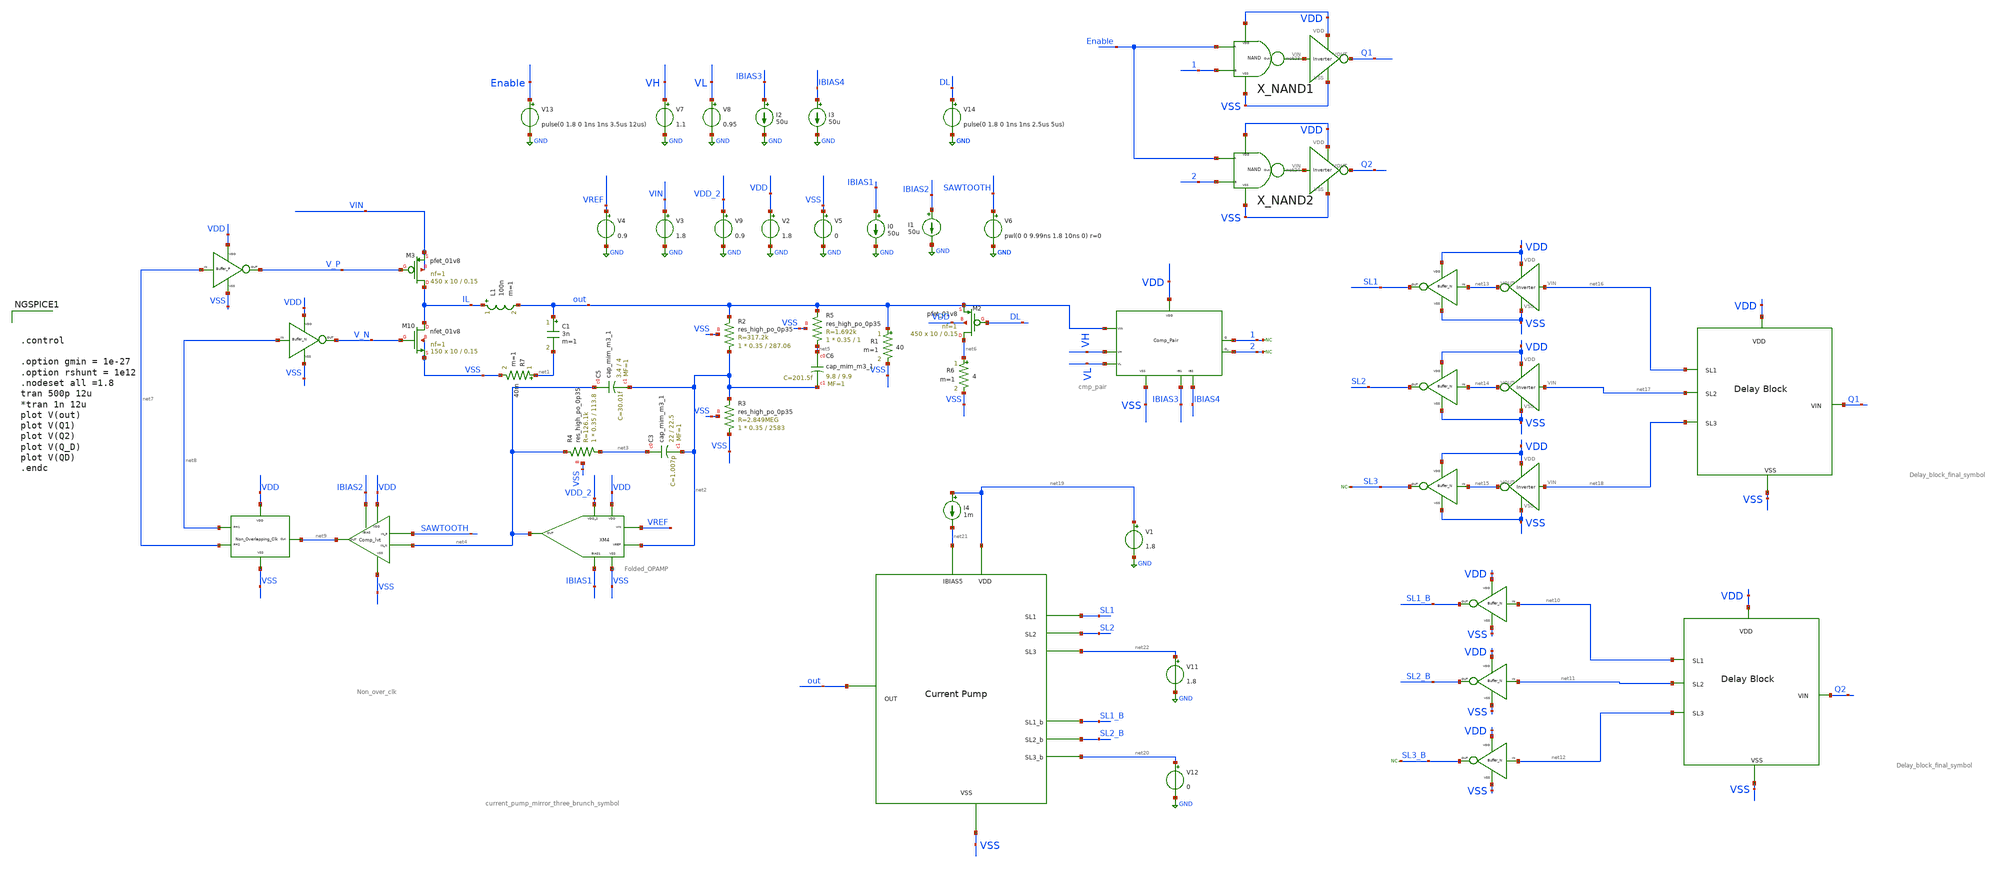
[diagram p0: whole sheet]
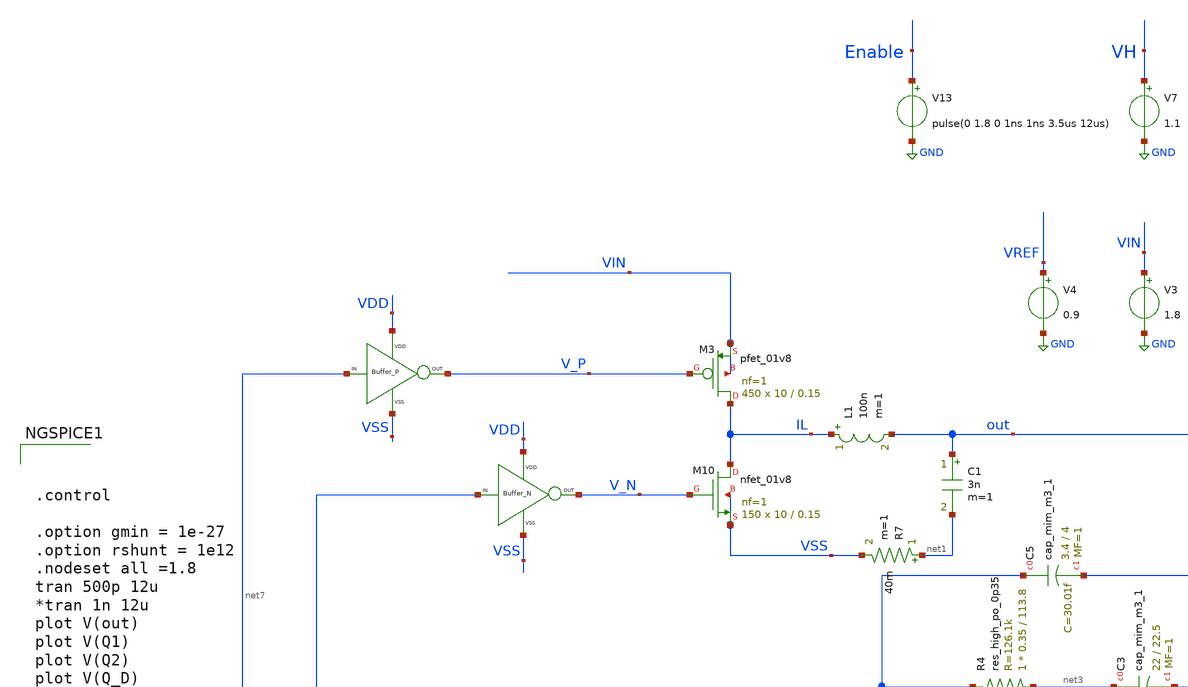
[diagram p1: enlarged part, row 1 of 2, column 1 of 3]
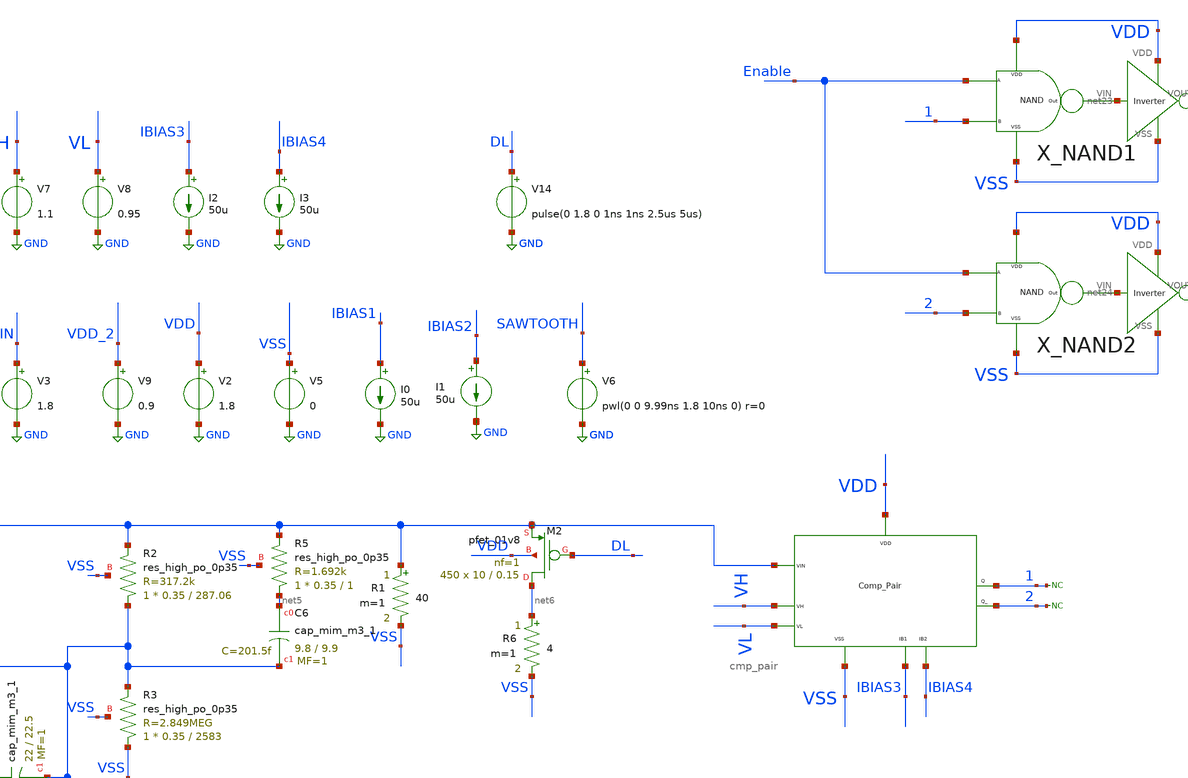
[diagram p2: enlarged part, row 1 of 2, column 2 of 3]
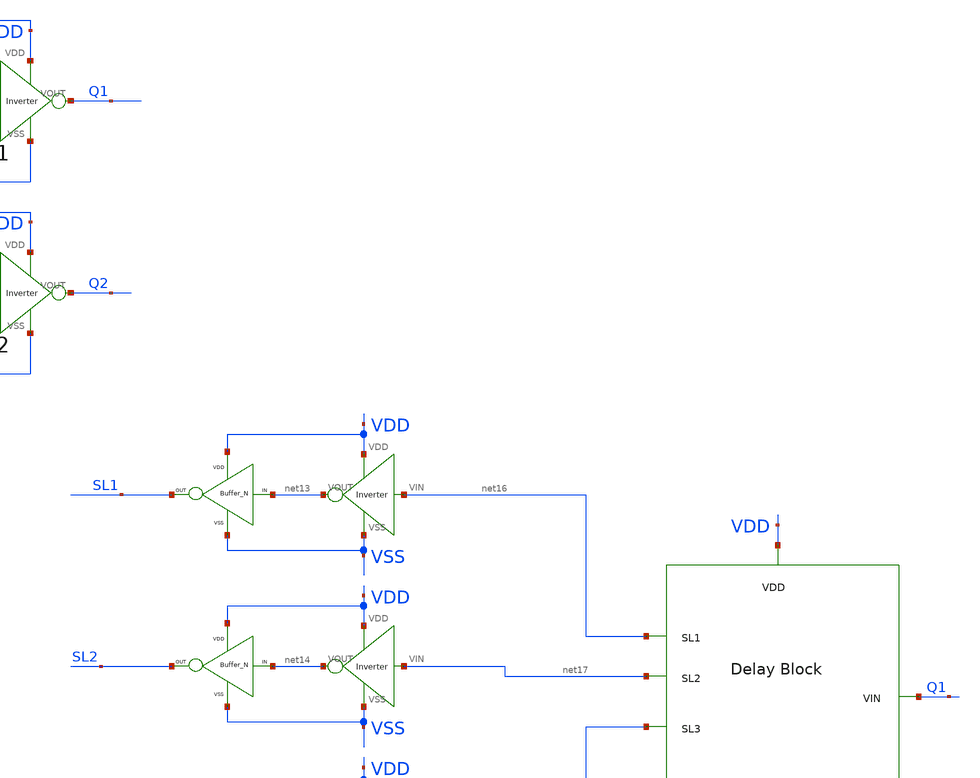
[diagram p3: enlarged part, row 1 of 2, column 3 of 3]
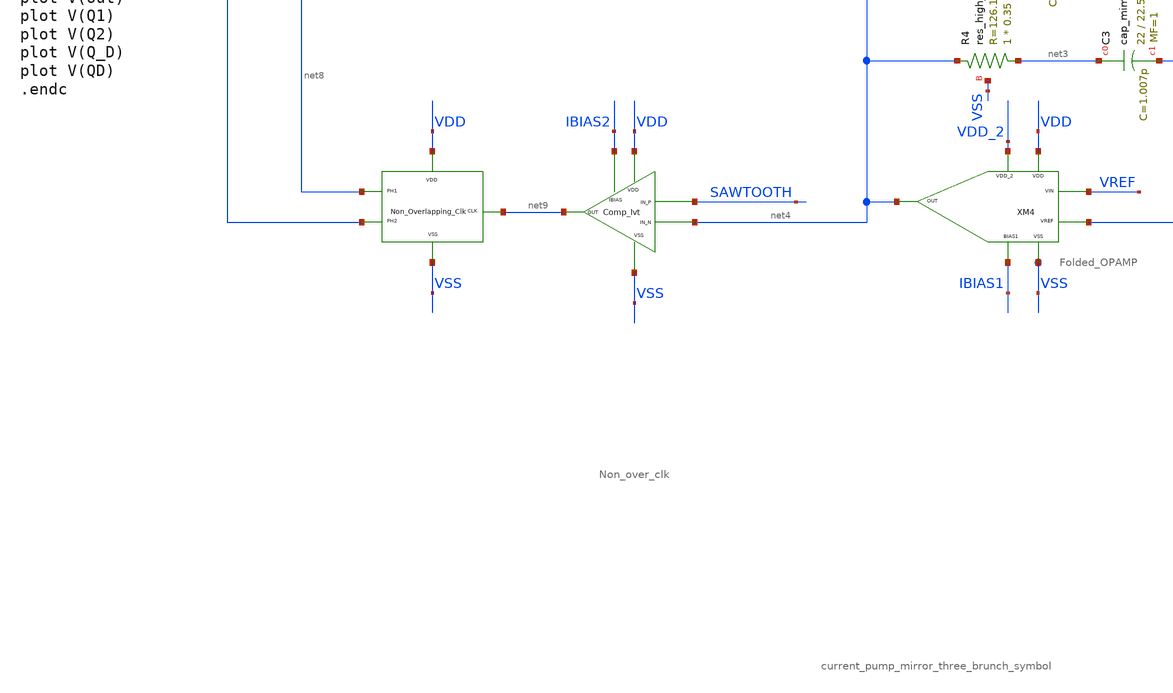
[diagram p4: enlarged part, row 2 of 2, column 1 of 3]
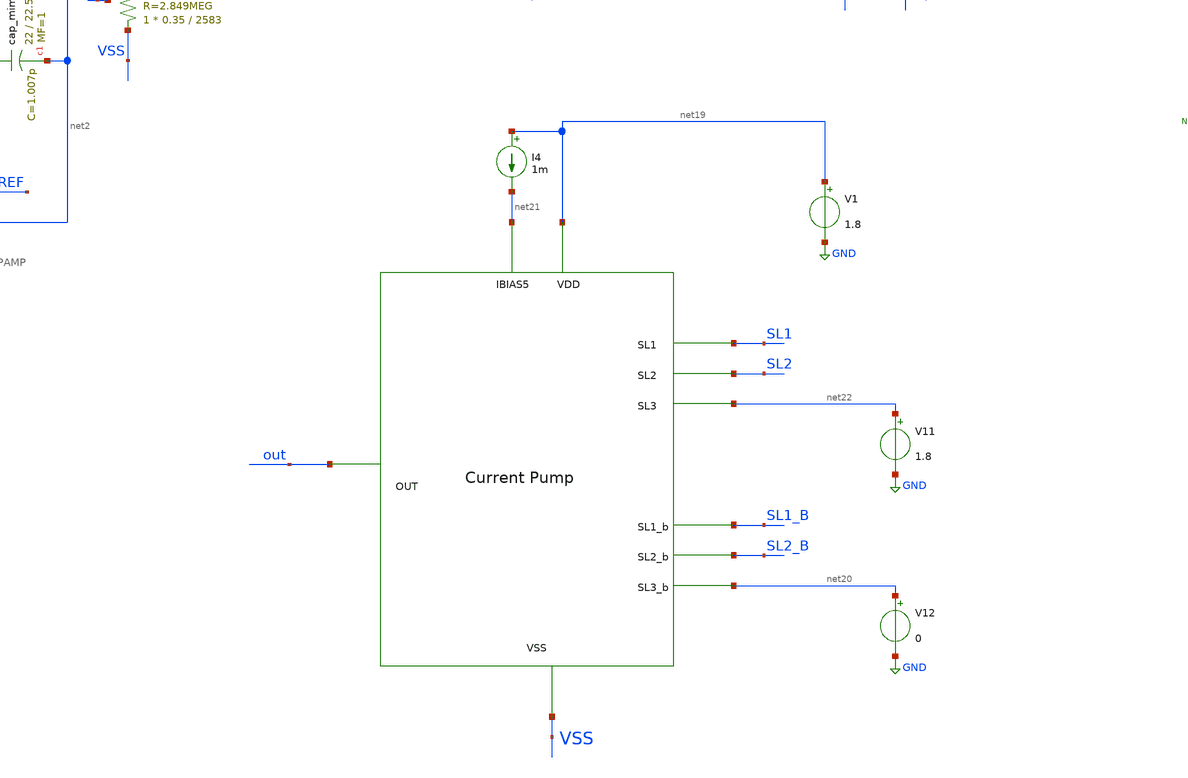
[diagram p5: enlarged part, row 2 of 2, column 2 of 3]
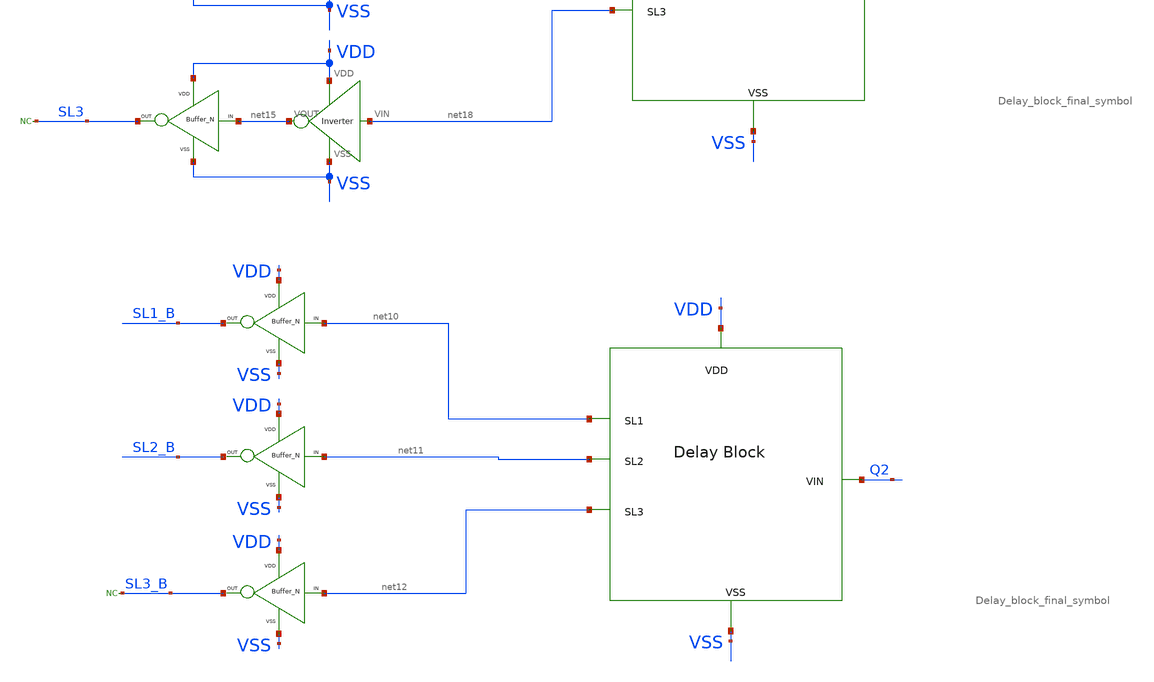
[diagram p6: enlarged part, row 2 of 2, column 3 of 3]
** sch_path: xschem/DC_DC_Converter_xschem/OTHERS/DC_DC_Converter_JV10/TOP_LEVEL/closed_loop_jd_sep_v4.sch
**.subckt closed_loop_jd_sep_v4
XM3 IL V_P VIN VIN sky130_fd_pr__pfet_01v8 L=0.15 W=10 nf=1 ad='int((nf+1)/2) * W/nf * 0.29' as='int((nf+2)/2) * W/nf * 0.29'
+ pd='2*int((nf+1)/2) * (W/nf + 0.29)' ps='2*int((nf+2)/2) * (W/nf + 0.29)' nrd='0.29 / W' nrs='0.29 / W'
+ sa=0 sb=0 sd=0 mult=450 m=450
L1 IL out 100n m=1
C1 out net1 3n m=1
V3 VIN GND 1.8
I0 IBIAS1 GND 50u
V9 VDD_2 GND 0.9
V2 VDD GND 1.8
V5 VSS GND 0
V4 VREF GND 0.9
I1 IBIAS2 GND 50u
V6 SAWTOOTH GND pwl(0 0 9.99ns 1.8 10ns 0) r=0
XM2 net6 DL out VDD sky130_fd_pr__pfet_01v8 L=0.15 W=10 nf=1 ad='int((nf+1)/2) * W/nf * 0.29' as='int((nf+2)/2) * W/nf * 0.29'
+ pd='2*int((nf+1)/2) * (W/nf + 0.29)' ps='2*int((nf+2)/2) * (W/nf + 0.29)' nrd='0.29 / W' nrs='0.29 / W'
+ sa=0 sb=0 sd=0 mult=450 m=450
X101 net7 V_P VDD VSS BUFFER_P
X2 net8 V_N VDD VSS BUFFER_N
XM3 VDD net9 net8 VSS net7 Non_over_clk
XM4 VDD VSS VDD_2 IBIAS1 net4 VREF net2 Folded_OPAMP
XC5 net4 net2 sky130_fd_pr__cap_mim_m3_1 W=3.4 L=4 MF=1 m=1
XC3 net3 net2 sky130_fd_pr__cap_mim_m3_1 W=22 L=22.5 MF=1 m=1
XC6 net5 net2 sky130_fd_pr__cap_mim_m3_1 W=9.8 L=9.9 MF=1 m=1
XM10 IL V_N VSS VSS sky130_fd_pr__nfet_01v8 L=0.15 W=10 nf=1 ad='int((nf+1)/2) * W/nf * 0.29' as='int((nf+2)/2) * W/nf * 0.29'
+ pd='2*int((nf+1)/2) * (W/nf + 0.29)' ps='2*int((nf+2)/2) * (W/nf + 0.29)' nrd='0.29 / W' nrs='0.29 / W'
+ sa=0 sb=0 sd=0 mult=150 m=150
XR4 net3 net4 VSS sky130_fd_pr__res_high_po_0p35 L=113.8 mult=1 m=1
XR5 net5 out VSS sky130_fd_pr__res_high_po_0p35 L=1 mult=1 m=1
XR2 net2 out VSS sky130_fd_pr__res_high_po_0p35 L=287.06 mult=1 m=1
XR3 VSS net2 VSS sky130_fd_pr__res_high_po_0p35 L=2583 mult=1 m=1
R7 net1 VSS 40m m=1
R1 out VSS 40 m=1
R6 net6 VSS 4 m=1
XM2 IBIAS2 VDD SAWTOOTH net4 VSS net9 Comp_lvt
XM1 VDD VSS out VH VL IBIAS3 IBIAS4 1 2 cmp_pair
V7 VH GND 1.1
V8 VL GND 0.95
I2 IBIAS3 GND 50u
I3 IBIAS4 GND 50u
* noconn 2
* noconn 1
X_NAND1 VDD VSS Enable 1 net23 NAND
X_NAND2 VDD VSS Enable 2 net24 NAND
X9 VSS VDD net23 Q1 Inverter
X10 VSS VDD net24 Q2 Inverter
x1 net11 net12 VDD Q2 VSS net10 Delay_block_final_symbol
x2 net17 net18 VDD Q1 VSS net16 Delay_block_final_symbol
X3 VSS VDD net16 net13 Inverter
X4 VSS VDD net17 net14 Inverter
X5 VSS VDD net18 net15 Inverter
x3 net19 net21 net22 out SL2 SL1 VSS net20 SL2_B SL1_B current_pump_mirror_three_brunch_symbol
I4 net19 net21 1m
X6 net14 SL2 VDD VSS BUFFER_N
X7 net15 SL3 VDD VSS BUFFER_N
X8 net13 SL1 VDD VSS BUFFER_N
X11 net11 SL2_B VDD VSS BUFFER_N
X12 net12 SL3_B VDD VSS BUFFER_N
X13 net10 SL1_B VDD VSS BUFFER_N
V1 net19 GND 1.8
V14 DL GND pulse(0 1.8 0 1ns 1ns 2.5us 5us)
V11 net22 GND 1.8
V12 net20 GND 0
* noconn SL3_B
* noconn SL3
V13 Enable GND pulse(0 1.8 0 1ns 1ns 3.5us 12us)
**** begin user architecture code

** opencircuitdesign pdks install
.lib $::SKYWATER_MODELS/sky130.lib.spice tt





.control

.option gmin = 1e-27
.option rshunt = 1e12
.nodeset all =1.8
tran 500p 12u
*tran 1n 12u
plot V(out)
plot V(Q1)
plot V(Q2)
plot V(Q_D)
plot V(QD)
.endc


**** end user architecture code
**.ends
.GLOBAL GND
.end
